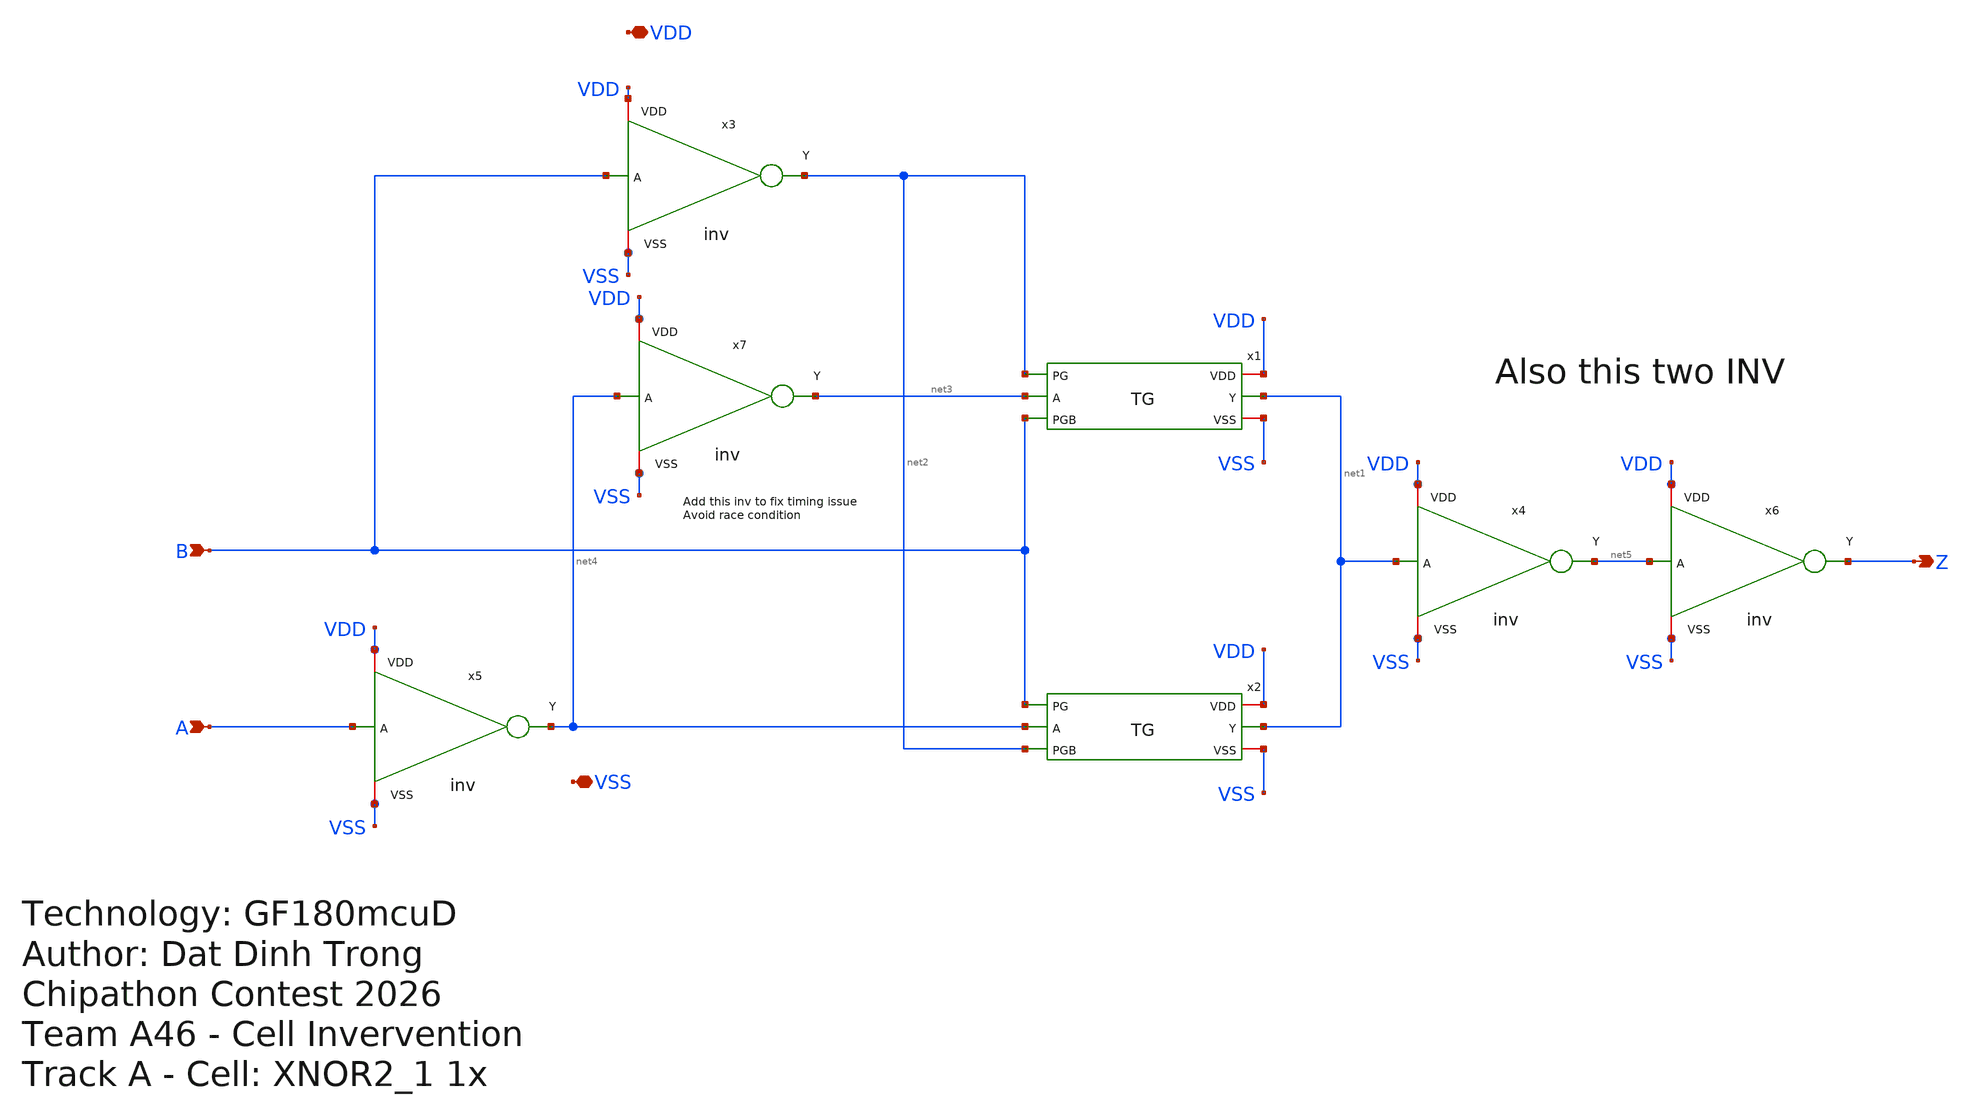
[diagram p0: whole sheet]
** sch_path: XNOR2_1.sch
**.subckt XNOR2_1 A B Z VDD VSS
*.ipin A
*.ipin B
*.opin Z
*.iopin VDD
*.iopin VSS
x1 net2 VDD net1 net3 VSS B TG
x2 B VDD net1 net4 VSS net2 TG
x3 VDD B net2 VSS inv
x5 VDD A net4 VSS inv
x4 VDD net1 net5 VSS inv
x6 VDD net5 Z VSS inv
x7 VDD net4 net3 VSS inv
**.ends
.end
